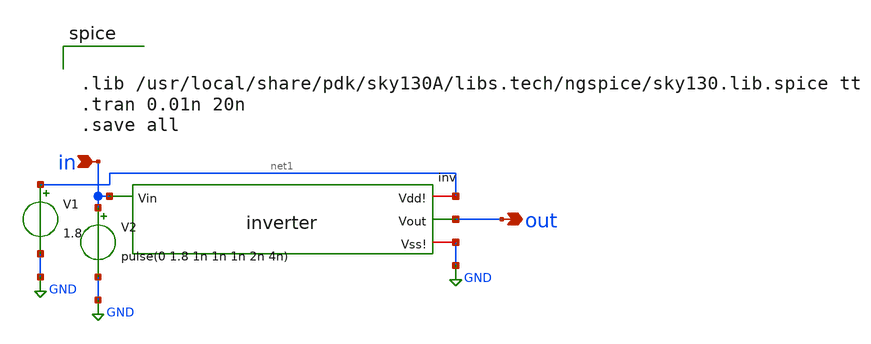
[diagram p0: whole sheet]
** sch_path: week2/inv/untitled.sch
**.subckt untitled out in
*.opin out
*.ipin in
x1 net1 in out GND inv
V1 net1 GND 1.8
V2 in GND pulse(0 1.8 1n 1n 1n 2n 4n)
**** begin user architecture code


.lib /usr/local/share/pdk/sky130A/libs.tech/ngspice/sky130.lib.spice tt
.tran 0.01n 20n
.save all


**** end user architecture code
**.ends

* expanding   symbol:  inv.sym # of pins=4
** sym_path: week2/inv/inv.sym
** sch_path: week2/inv/inv.sch
.subckt inv Vdd! Vin Vout Vss!
*.ipin Vin
*.opin Vout
*.iopin Vdd!
*.iopin Vss!
XM1 Vout Vin Vdd! Vdd! sky130_fd_pr__pfet_01v8 L=0.15 W=1 nf=1 ad='int((nf+1)/2) * W/nf * 0.29' as='int((nf+2)/2) * W/nf * 0.29'
+ pd='2*int((nf+1)/2) * (W/nf + 0.29)' ps='2*int((nf+2)/2) * (W/nf + 0.29)' nrd='0.29 / W' nrs='0.29 / W'
+ sa=0 sb=0 sd=0 mult=1 m=1
XM2 Vout Vin Vss! Vss! sky130_fd_pr__nfet_01v8 L=0.15 W=1 nf=1 ad='int((nf+1)/2) * W/nf * 0.29' as='int((nf+2)/2) * W/nf * 0.29'
+ pd='2*int((nf+1)/2) * (W/nf + 0.29)' ps='2*int((nf+2)/2) * (W/nf + 0.29)' nrd='0.29 / W' nrs='0.29 / W'
+ sa=0 sb=0 sd=0 mult=1 m=1
.ends

.GLOBAL GND
.end
